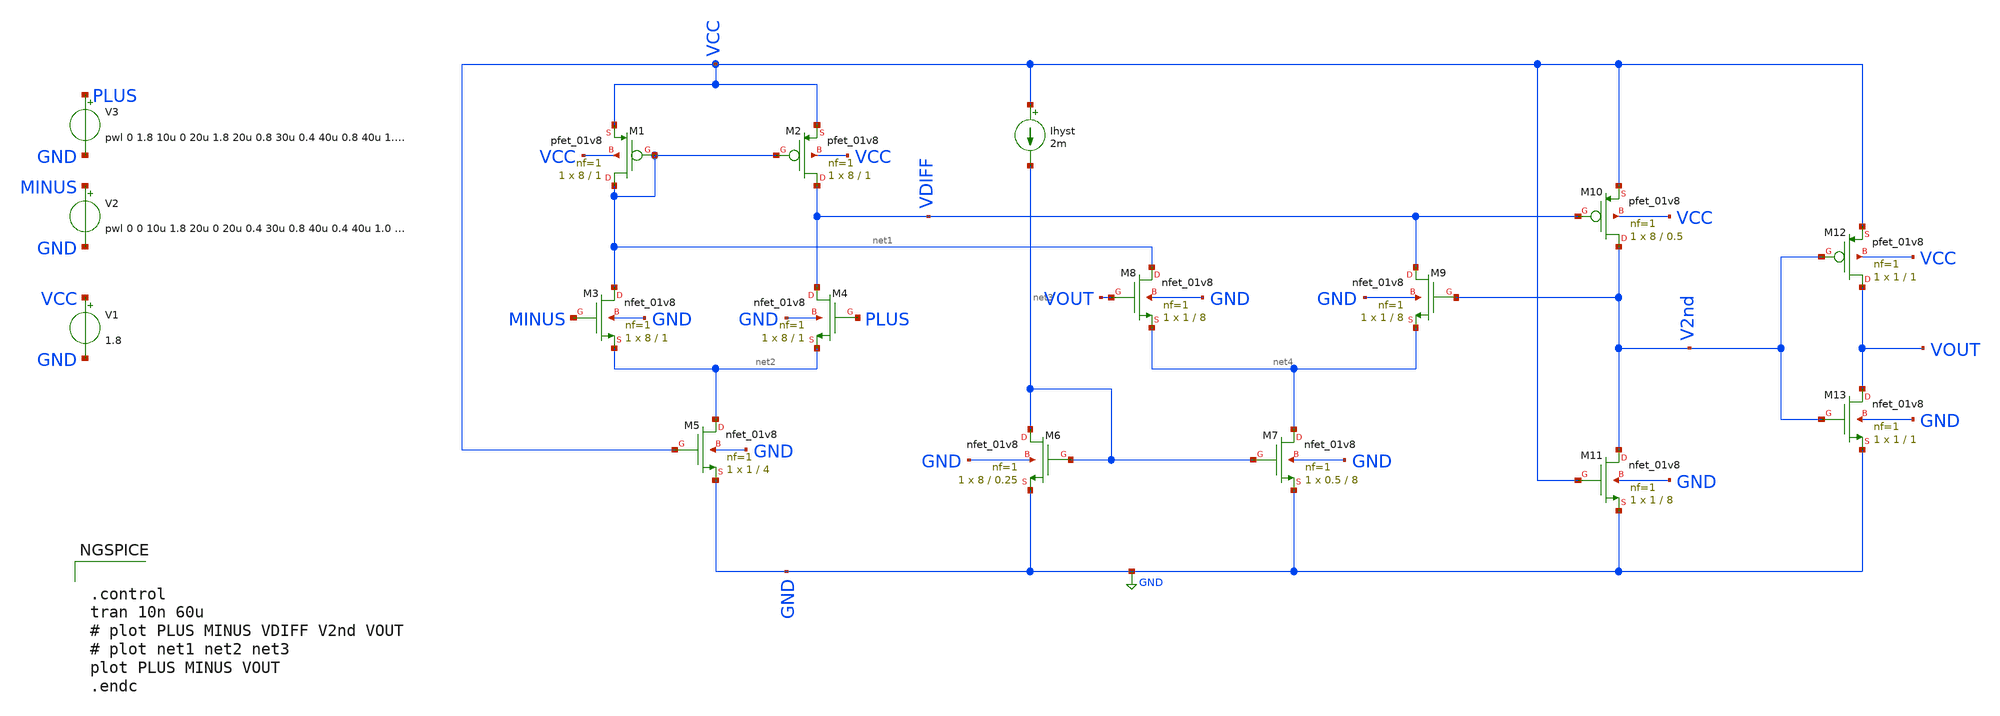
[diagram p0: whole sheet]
** sch_path: PreLayout/archive/comparator_1v8.sch
* Copyright 2020 Stefan Frederik Schippers
* Licensed under the Apache License, Version 2.0 (the "License");
* you may not use this file except in compliance with the License.
* You may obtain a copy of the License at
* https://www.apache.org/licenses/LICENSE-2.0
* Unless required by applicable law or agreed to in writing, software
* distributed under the License is distributed on an "AS IS" BASIS,
* WITHOUT WARRANTIES OR CONDITIONS OF ANY KIND, either express or implied.
* See the License for the specific language governing permissions and
* limitations under the License.
**.subckt comparator_1v8
XM2 VDIFF net1 VCC VCC sky130_fd_pr__pfet_01v8 L=1 W=8 nf=1 ad='int((nf+1)/2) * W/nf * 0.29' as='int((nf+2)/2) * W/nf * 0.29'
+ pd='2*int((nf+1)/2) * (W/nf + 0.29)' ps='2*int((nf+2)/2) * (W/nf + 0.29)' nrd='0.29 / W' nrs='0.29 / W'
+ sa=0 sb=0 sd=0 mult=1 m=1
XM1 net1 net1 VCC VCC sky130_fd_pr__pfet_01v8 L=1 W=8 nf=1 ad='int((nf+1)/2) * W/nf * 0.29' as='int((nf+2)/2) * W/nf * 0.29'
+ pd='2*int((nf+1)/2) * (W/nf + 0.29)' ps='2*int((nf+2)/2) * (W/nf + 0.29)' nrd='0.29 / W' nrs='0.29 / W'
+ sa=0 sb=0 sd=0 mult=1 m=1
XM5 net2 VCC GND GND sky130_fd_pr__nfet_01v8 L=4 W=1 nf=1 ad='int((nf+1)/2) * W/nf * 0.29' as='int((nf+2)/2) * W/nf * 0.29'
+ pd='2*int((nf+1)/2) * (W/nf + 0.29)' ps='2*int((nf+2)/2) * (W/nf + 0.29)' nrd='0.29 / W' nrs='0.29 / W'
+ sa=0 sb=0 sd=0 mult=1 m=1
XM4 VDIFF PLUS net2 GND sky130_fd_pr__nfet_01v8 L=1 W=8 nf=1 ad='int((nf+1)/2) * W/nf * 0.29' as='int((nf+2)/2) * W/nf * 0.29'
+ pd='2*int((nf+1)/2) * (W/nf + 0.29)' ps='2*int((nf+2)/2) * (W/nf + 0.29)' nrd='0.29 / W' nrs='0.29 / W'
+ sa=0 sb=0 sd=0 mult=1 m=1
XM3 net1 MINUS net2 GND sky130_fd_pr__nfet_01v8 L=1 W=8 nf=1 ad='int((nf+1)/2) * W/nf * 0.29' as='int((nf+2)/2) * W/nf * 0.29'
+ pd='2*int((nf+1)/2) * (W/nf + 0.29)' ps='2*int((nf+2)/2) * (W/nf + 0.29)' nrd='0.29 / W' nrs='0.29 / W'
+ sa=0 sb=0 sd=0 mult=1 m=1
XM7 net4 net3 GND GND sky130_fd_pr__nfet_01v8 L=8 W=0.5 nf=1 ad='int((nf+1)/2) * W/nf * 0.29' as='int((nf+2)/2) * W/nf * 0.29'
+ pd='2*int((nf+1)/2) * (W/nf + 0.29)' ps='2*int((nf+2)/2) * (W/nf + 0.29)' nrd='0.29 / W' nrs='0.29 / W'
+ sa=0 sb=0 sd=0 mult=1 m=1
XM6 net3 net3 GND GND sky130_fd_pr__nfet_01v8 L=0.25 W=8 nf=1 ad='int((nf+1)/2) * W/nf * 0.29' as='int((nf+2)/2) * W/nf * 0.29'
+ pd='2*int((nf+1)/2) * (W/nf + 0.29)' ps='2*int((nf+2)/2) * (W/nf + 0.29)' nrd='0.29 / W' nrs='0.29 / W'
+ sa=0 sb=0 sd=0 mult=1 m=1
XM8 net1 VOUT net4 GND sky130_fd_pr__nfet_01v8 L=8 W=1 nf=1 ad='int((nf+1)/2) * W/nf * 0.29' as='int((nf+2)/2) * W/nf * 0.29'
+ pd='2*int((nf+1)/2) * (W/nf + 0.29)' ps='2*int((nf+2)/2) * (W/nf + 0.29)' nrd='0.29 / W' nrs='0.29 / W'
+ sa=0 sb=0 sd=0 mult=1 m=1
XM9 VDIFF V2nd net4 GND sky130_fd_pr__nfet_01v8 L=8 W=1 nf=1 ad='int((nf+1)/2) * W/nf * 0.29' as='int((nf+2)/2) * W/nf * 0.29'
+ pd='2*int((nf+1)/2) * (W/nf + 0.29)' ps='2*int((nf+2)/2) * (W/nf + 0.29)' nrd='0.29 / W' nrs='0.29 / W'
+ sa=0 sb=0 sd=0 mult=1 m=1
XM10 V2nd VDIFF VCC VCC sky130_fd_pr__pfet_01v8 L=0.5 W=8 nf=1 ad='int((nf+1)/2) * W/nf * 0.29' as='int((nf+2)/2) * W/nf * 0.29'
+ pd='2*int((nf+1)/2) * (W/nf + 0.29)' ps='2*int((nf+2)/2) * (W/nf + 0.29)' nrd='0.29 / W' nrs='0.29 / W'
+ sa=0 sb=0 sd=0 mult=1 m=1
XM11 V2nd VCC GND GND sky130_fd_pr__nfet_01v8 L=8 W=1 nf=1 ad='int((nf+1)/2) * W/nf * 0.29' as='int((nf+2)/2) * W/nf * 0.29'
+ pd='2*int((nf+1)/2) * (W/nf + 0.29)' ps='2*int((nf+2)/2) * (W/nf + 0.29)' nrd='0.29 / W' nrs='0.29 / W'
+ sa=0 sb=0 sd=0 mult=1 m=1
XM12 VOUT V2nd VCC VCC sky130_fd_pr__pfet_01v8 L=1 W=1 nf=1 ad='int((nf+1)/2) * W/nf * 0.29' as='int((nf+2)/2) * W/nf * 0.29'
+ pd='2*int((nf+1)/2) * (W/nf + 0.29)' ps='2*int((nf+2)/2) * (W/nf + 0.29)' nrd='0.29 / W' nrs='0.29 / W'
+ sa=0 sb=0 sd=0 mult=1 m=1
XM13 VOUT V2nd GND GND sky130_fd_pr__nfet_01v8 L=1 W=1 nf=1 ad='int((nf+1)/2) * W/nf * 0.29' as='int((nf+2)/2) * W/nf * 0.29'
+ pd='2*int((nf+1)/2) * (W/nf + 0.29)' ps='2*int((nf+2)/2) * (W/nf + 0.29)' nrd='0.29 / W' nrs='0.29 / W'
+ sa=0 sb=0 sd=0 mult=1 m=1
Ihyst VCC net3 2m
V1 VCC GND 1.8
V2 MINUS GND pwl 0 0 10u 1.8 20u 0 20u 0.4 30u 0.8 40u 0.4 40u 1.0 50u 1.4 60u 1.0
V3 PLUS GND pwl 0 1.8 10u 0 20u 1.8 20u 0.8 30u 0.4 40u 0.8 40u 1.4 50u 1.0 60u 1.4
**** begin user architecture code

.include $::SKYWATER_MODELS/cells/nfet_01v8/sky130_fd_pr__nfet_01v8__tt.corner.spice
.include $::SKYWATER_MODELS/cells/nfet_01v8_lvt/sky130_fd_pr__nfet_01v8_lvt__tt.corner.spice
.include $::SKYWATER_MODELS/cells/pfet_01v8/sky130_fd_pr__pfet_01v8__tt.corner.spice
.include $::SKYWATER_MODELS/cells/nfet_03v3_nvt/sky130_fd_pr__nfet_03v3_nvt__tt.corner.spice
.include $::SKYWATER_MODELS/cells/nfet_05v0_nvt/sky130_fd_pr__nfet_05v0_nvt__tt.corner.spice
.include $::SKYWATER_MODELS/cells/esd_nfet_01v8/sky130_fd_pr__esd_nfet_01v8__tt.corner.spice
.include $::SKYWATER_MODELS/cells/pfet_01v8_lvt/sky130_fd_pr__pfet_01v8_lvt__tt.corner.spice
.include $::SKYWATER_MODELS/cells/pfet_01v8_hvt/sky130_fd_pr__pfet_01v8_hvt__tt.corner.spice
.include $::SKYWATER_MODELS/cells/esd_pfet_g5v0d10v5/sky130_fd_pr__esd_pfet_g5v0d10v5__tt.corner.spice
.include $::SKYWATER_MODELS/cells/pfet_g5v0d10v5/sky130_fd_pr__pfet_g5v0d10v5__tt.corner.spice
.include $::SKYWATER_MODELS/cells/pfet_g5v0d16v0/sky130_fd_pr__pfet_g5v0d16v0__tt.corner.spice
.include $::SKYWATER_MODELS/cells/nfet_g5v0d10v5/sky130_fd_pr__nfet_g5v0d10v5__tt.corner.spice
.include $::SKYWATER_MODELS/cells/nfet_g5v0d16v0/sky130_fd_pr__nfet_g5v0d16v0__tt_discrete.corner.spice
.include $::SKYWATER_MODELS/cells/esd_nfet_g5v0d10v5/sky130_fd_pr__esd_nfet_g5v0d10v5__tt.corner.spice
.include $::SKYWATER_MODELS/models/corners/tt/nonfet.spice
* Mismatch parameters
.include $::SKYWATER_MODELS/cells/nfet_01v8/sky130_fd_pr__nfet_01v8__mismatch.corner.spice
.include $::SKYWATER_MODELS/cells/pfet_01v8/sky130_fd_pr__pfet_01v8__mismatch.corner.spice
.include $::SKYWATER_MODELS/cells/nfet_01v8_lvt/sky130_fd_pr__nfet_01v8_lvt__mismatch.corner.spice
.include $::SKYWATER_MODELS/cells/pfet_01v8_lvt/sky130_fd_pr__pfet_01v8_lvt__mismatch.corner.spice
.include $::SKYWATER_MODELS/cells/pfet_01v8_hvt/sky130_fd_pr__pfet_01v8_hvt__mismatch.corner.spice
.include $::SKYWATER_MODELS/cells/nfet_g5v0d10v5/sky130_fd_pr__nfet_g5v0d10v5__mismatch.corner.spice
.include $::SKYWATER_MODELS/cells/pfet_g5v0d10v5/sky130_fd_pr__pfet_g5v0d10v5__mismatch.corner.spice
.include $::SKYWATER_MODELS/cells/nfet_05v0_nvt/sky130_fd_pr__nfet_05v0_nvt__mismatch.corner.spice
.include $::SKYWATER_MODELS/cells/nfet_03v3_nvt/sky130_fd_pr__nfet_03v3_nvt__mismatch.corner.spice
* Resistor$::SKYWATER_MODELS/Capacitor
.include $::SKYWATER_MODELS/models/r+c/res_typical__cap_typical.spice
.include $::SKYWATER_MODELS/models/r+c/res_typical__cap_typical__lin.spice
* Special cells
.include $::SKYWATER_MODELS/models/corners/tt/specialized_cells.spice
* All models
.include $::SKYWATER_MODELS/models/all.spice
* Corner
.include $::SKYWATER_MODELS/models/corners/tt/rf.spice



.control
tran 10n 60u
# plot PLUS MINUS VDIFF V2nd VOUT
# plot net1 net2 net3
plot PLUS MINUS VOUT
.endc


**** end user architecture code
**.ends
.GLOBAL GND
.end
